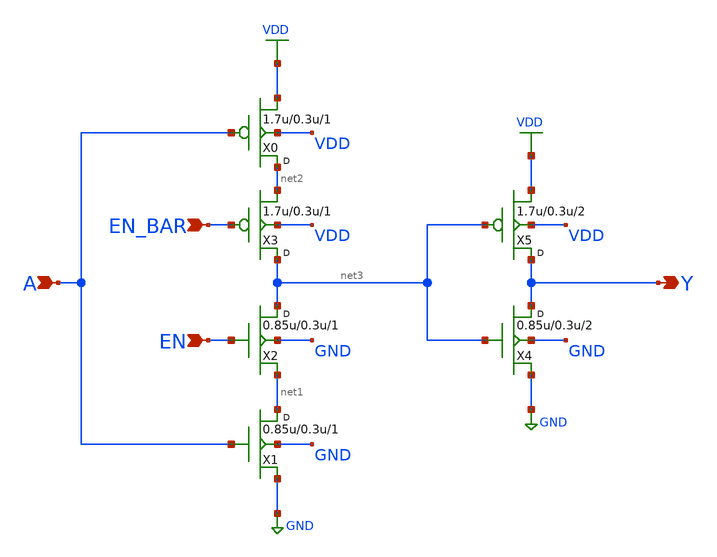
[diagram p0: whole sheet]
** sch_path: gf180mcu_osu_sc_gp9t3v3/cells/tbuf/gf180mcu_osu_sc_gp9t3v3__tbuf_2.sch
**.subckt gf180mcu_osu_sc_gp9t3v3__tbuf_2 A Y EN_BAR EN
*.ipin A
*.opin Y
*.ipin EN_BAR
*.ipin EN
X0 net2 A VDD VDD pmos_3p3 w=1.7u l=0.3u m=1
X1 net1 A GND GND nmos_3p3 w=0.85u l=0.3u m=1
X2 net3 EN net1 GND nmos_3p3 w=0.85u l=0.3u m=1
X3 net3 EN_BAR net2 VDD pmos_3p3 w=1.7u l=0.3u m=1
X4 Y net3 GND GND nmos_3p3 w=0.85u l=0.3u m=2
X5 Y net3 VDD VDD pmos_3p3 w=1.7u l=0.3u m=2
**.ends
.GLOBAL VDD
.GLOBAL GND
.end
